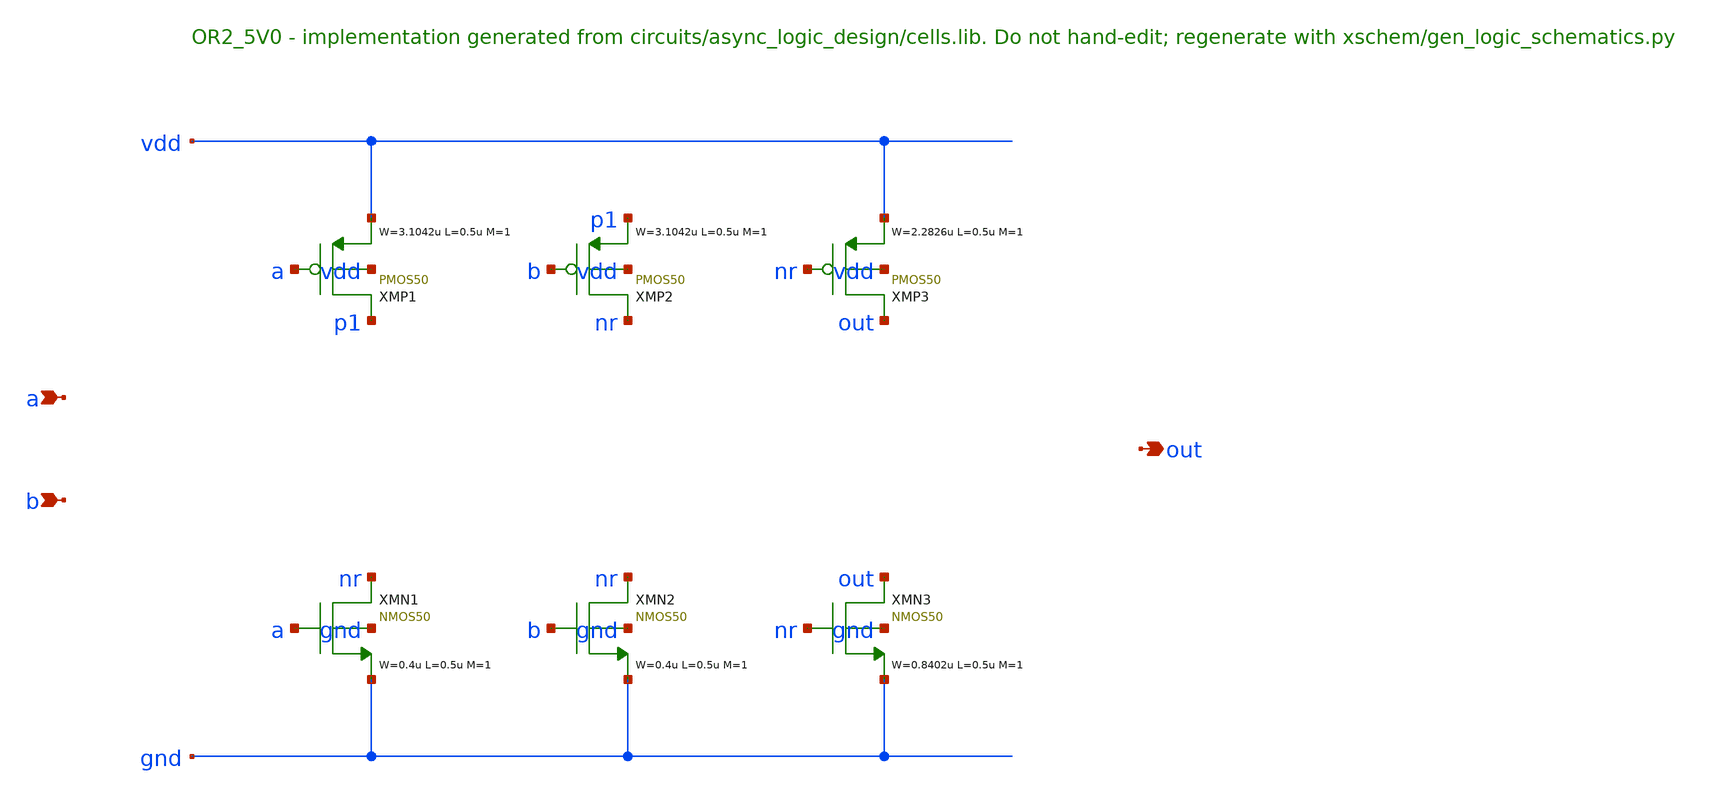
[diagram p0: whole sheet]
** sch_path: xschem/logic/OR2_5V0.sch
**.subckt OR2_5V0 a b out
*.ipin a
*.ipin b
*.opin out
XMP1 p1 a vdd vdd PMOS50 W=3.1042u L=0.5u M=1 MM_SIGMA=0
XMP2 nr b p1 vdd PMOS50 W=3.1042u L=0.5u M=1 MM_SIGMA=0
XMP3 out nr vdd vdd PMOS50 W=2.2826u L=0.5u M=1 MM_SIGMA=0
XMN1 nr a gnd gnd NMOS50 W=0.4u L=0.5u M=1 MM_SIGMA=0
XMN2 nr b gnd gnd NMOS50 W=0.4u L=0.5u M=1 MM_SIGMA=0
XMN3 out nr gnd gnd NMOS50 W=0.8402u L=0.5u M=1 MM_SIGMA=0
**.ends
.end
